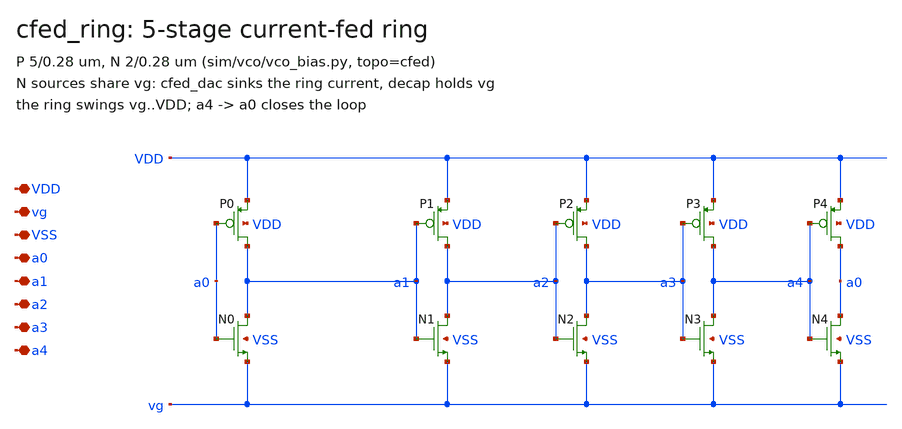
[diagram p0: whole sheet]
** sch_path: xschem/cfed_ring.sch
**.subckt cfed_ring VDD vg VSS a0 a1 a2 a3 a4
*.iopin VDD
*.iopin vg
*.iopin VSS
*.iopin a0
*.iopin a1
*.iopin a2
*.iopin a3
*.iopin a4
XP0 a1 a0 VDD VDD pfet_03v3 L=0.28u W=5.0u nf=1 ad=2.5p as=2.5p pd=11.0u ps=11.0u nrd=0 nrs=0 sa=0
+ sb=0 sd=0 m=1
XN0 a1 a0 vg VSS nfet_03v3 L=0.28u W=2.0u nf=1 ad=1.0p as=1.0p pd=5.0u ps=5.0u nrd=0 nrs=0 sa=0 sb=0
+ sd=0 m=1
XP1 a2 a1 VDD VDD pfet_03v3 L=0.28u W=5.0u nf=1 ad=2.5p as=2.5p pd=11.0u ps=11.0u nrd=0 nrs=0 sa=0
+ sb=0 sd=0 m=1
XN1 a2 a1 vg VSS nfet_03v3 L=0.28u W=2.0u nf=1 ad=1.0p as=1.0p pd=5.0u ps=5.0u nrd=0 nrs=0 sa=0 sb=0
+ sd=0 m=1
XP2 a3 a2 VDD VDD pfet_03v3 L=0.28u W=5.0u nf=1 ad=2.5p as=2.5p pd=11.0u ps=11.0u nrd=0 nrs=0 sa=0
+ sb=0 sd=0 m=1
XN2 a3 a2 vg VSS nfet_03v3 L=0.28u W=2.0u nf=1 ad=1.0p as=1.0p pd=5.0u ps=5.0u nrd=0 nrs=0 sa=0 sb=0
+ sd=0 m=1
XP3 a4 a3 VDD VDD pfet_03v3 L=0.28u W=5.0u nf=1 ad=2.5p as=2.5p pd=11.0u ps=11.0u nrd=0 nrs=0 sa=0
+ sb=0 sd=0 m=1
XN3 a4 a3 vg VSS nfet_03v3 L=0.28u W=2.0u nf=1 ad=1.0p as=1.0p pd=5.0u ps=5.0u nrd=0 nrs=0 sa=0 sb=0
+ sd=0 m=1
XP4 a0 a4 VDD VDD pfet_03v3 L=0.28u W=5.0u nf=1 ad=2.5p as=2.5p pd=11.0u ps=11.0u nrd=0 nrs=0 sa=0
+ sb=0 sd=0 m=1
XN4 a0 a4 vg VSS nfet_03v3 L=0.28u W=2.0u nf=1 ad=1.0p as=1.0p pd=5.0u ps=5.0u nrd=0 nrs=0 sa=0 sb=0
+ sd=0 m=1
**.ends
.end
